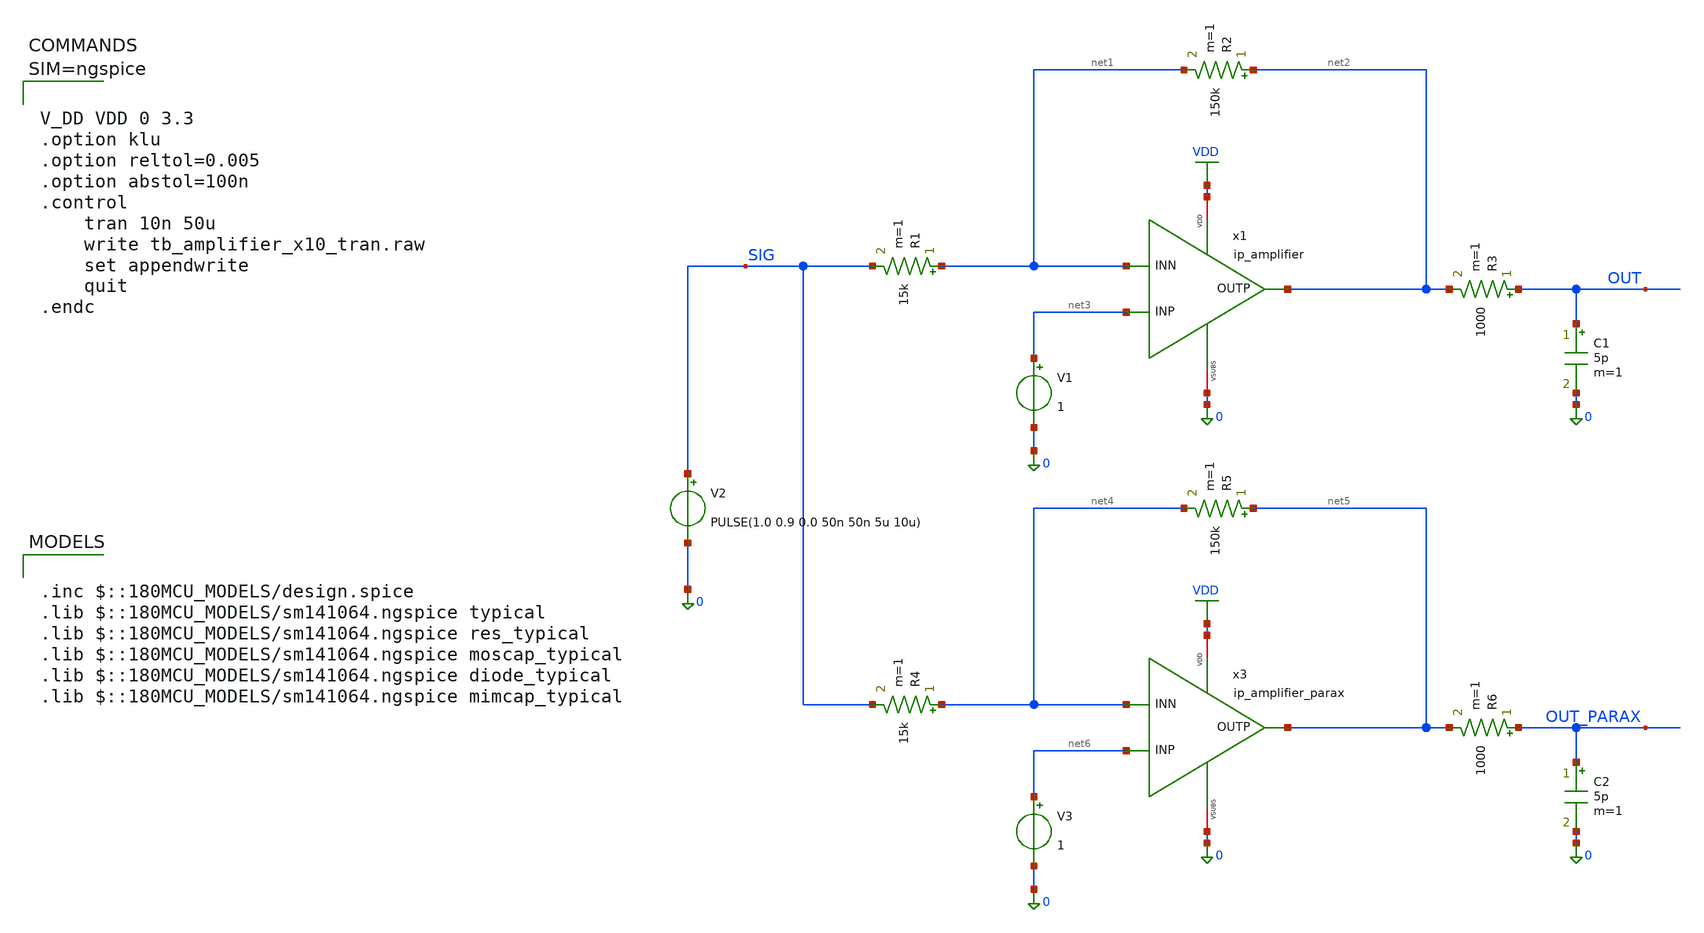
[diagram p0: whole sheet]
** sch_path: xschem/tb_amplifier_x10_tran.sch
**.subckt tb_amplifier_x10_tran
V2 SIG 0 PULSE(1.0 0.9 0.0 50n 50n 5u 10u)
x1 VDD 0 net3 net1 net2 ip_amplifier
R1 net1 SIG 15k m=1
R2 net2 net1 150k m=1
V1 net3 0 1
R3 OUT net2 1000 m=1
C1 OUT 0 5p m=1
R4 net4 SIG 15k m=1
R5 net5 net4 150k m=1
V3 net6 0 1
R6 OUT_PARAX net5 1000 m=1
C2 OUT_PARAX 0 5p m=1
x3 VDD 0 net6 net4 net5 ip_amplifier_parax
**** begin user architecture code

.inc $::180MCU_MODELS/design.spice
.lib $::180MCU_MODELS/sm141064.ngspice typical
.lib $::180MCU_MODELS/sm141064.ngspice res_typical
.lib $::180MCU_MODELS/sm141064.ngspice moscap_typical
.lib $::180MCU_MODELS/sm141064.ngspice diode_typical
.lib $::180MCU_MODELS/sm141064.ngspice mimcap_typical




V_DD VDD 0 3.3
.option klu
.option reltol=0.005
.option abstol=100n
.control
	tran 10n 50u
	write tb_amplifier_x10_tran.raw
	set appendwrite
	quit
.endc



**** end user architecture code
**.ends

* expanding   symbol:  ip_amplifier.sym # of pins=5
** sym_path: ip_amplifier.sym
** sch_path: ip_amplifier.sch
.subckt ip_amplifier VDD VSUBS INP INN OUTP
*.iopin VDD
*.iopin VSUBS
*.ipin INP
*.ipin INN
*.opin OUTP
XM1 COMP INP COMMON_ VDD pfet_03v3 L=5u W=18.0u nf=1 ad='int((nf+1)/2) * W/nf * 0.18u' as='int((nf+2)/2) * W/nf * 0.18u'
+ pd='2*int((nf+1)/2) * (W/nf + 0.18u)' ps='2*int((nf+2)/2) * (W/nf + 0.18u)' nrd='0.18u / W' nrs='0.18u / W'
+ sa=0 sb=0 sd=0 m=1 par=1
XM2 net6 INN COMMON_ VDD pfet_03v3 L=5u W=18.0u nf=1 ad='int((nf+1)/2) * W/nf * 0.18u' as='int((nf+2)/2) * W/nf * 0.18u'
+ pd='2*int((nf+1)/2) * (W/nf + 0.18u)' ps='2*int((nf+2)/2) * (W/nf + 0.18u)' nrd='0.18u / W' nrs='0.18u / W'
+ sa=0 sb=0 sd=0 m=1 par=1
XM3 net2 NBIAS VSUBS vsubs nfet_03v3 L=2u W=6u nf=1 ad='int((nf+1)/2) * W/nf * 0.18u' as='int((nf+2)/2) * W/nf * 0.18u'
+ pd='2*int((nf+1)/2) * (W/nf + 0.18u)' ps='2*int((nf+2)/2) * (W/nf + 0.18u)' nrd='0.18u / W' nrs='0.18u / W'
+ sa=0 sb=0 sd=0 m=2 par=2
XM4 net1 NBIAS VSUBS vsubs nfet_03v3 L=2u W=6u nf=1 ad='int((nf+1)/2) * W/nf * 0.18u' as='int((nf+2)/2) * W/nf * 0.18u'
+ pd='2*int((nf+1)/2) * (W/nf + 0.18u)' ps='2*int((nf+2)/2) * (W/nf + 0.18u)' nrd='0.18u / W' nrs='0.18u / W'
+ sa=0 sb=0 sd=0 m=1 par=1
XM7 NBIAS NBIAS net2 vsubs nfet_03v3 L=0.5u W=6u nf=1 ad='int((nf+1)/2) * W/nf * 0.18u' as='int((nf+2)/2) * W/nf * 0.18u'
+ pd='2*int((nf+1)/2) * (W/nf + 0.18u)' ps='2*int((nf+2)/2) * (W/nf + 0.18u)' nrd='0.18u / W' nrs='0.18u / W'
+ sa=0 sb=0 sd=0 m=4 par=4
XM8 net3 NBIAS net1 vsubs nfet_03v3 L=0.5u W=6u nf=1 ad='int((nf+1)/2) * W/nf * 0.18u' as='int((nf+2)/2) * W/nf * 0.18u'
+ pd='2*int((nf+1)/2) * (W/nf + 0.18u)' ps='2*int((nf+2)/2) * (W/nf + 0.18u)' nrd='0.18u / W' nrs='0.18u / W'
+ sa=0 sb=0 sd=0 m=4 par=4
XM9 net4 PBIAS VDD VDD pfet_03v3 L=2u W=6u nf=1 ad='int((nf+1)/2) * W/nf * 0.18u' as='int((nf+2)/2) * W/nf * 0.18u'
+ pd='2*int((nf+1)/2) * (W/nf + 0.18u)' ps='2*int((nf+2)/2) * (W/nf + 0.18u)' nrd='0.18u / W' nrs='0.18u / W'
+ sa=0 sb=0 sd=0 m=1 par=1
XM10 net5 PBIAS VDD VDD pfet_03v3 L=2u W=6u nf=1 ad='int((nf+1)/2) * W/nf * 0.18u' as='int((nf+2)/2) * W/nf * 0.18u'
+ pd='2*int((nf+1)/2) * (W/nf + 0.18u)' ps='2*int((nf+2)/2) * (W/nf + 0.18u)' nrd='0.18u / W' nrs='0.18u / W'
+ sa=0 sb=0 sd=0 m=1 par=1
XM11 PBIAS PBIAS net4 VDD pfet_03v3 L=0.5u W=6u nf=1 ad='int((nf+1)/2) * W/nf * 0.18u' as='int((nf+2)/2) * W/nf * 0.18u'
+ pd='2*int((nf+1)/2) * (W/nf + 0.18u)' ps='2*int((nf+2)/2) * (W/nf + 0.18u)' nrd='0.18u / W' nrs='0.18u / W'
+ sa=0 sb=0 sd=0 m=4 par=4
XM12 COMMON PBIAS net5 VDD pfet_03v3 L=0.5u W=6u nf=1 ad='int((nf+1)/2) * W/nf * 0.18u' as='int((nf+2)/2) * W/nf * 0.18u'
+ pd='2*int((nf+1)/2) * (W/nf + 0.18u)' ps='2*int((nf+2)/2) * (W/nf + 0.18u)' nrd='0.18u / W' nrs='0.18u / W'
+ sa=0 sb=0 sd=0 m=4 par=4
XM13 COMP net6 VSUBS vsubs nfet_03v3 L=5u W=6u nf=1 ad='int((nf+1)/2) * W/nf * 0.18u' as='int((nf+2)/2) * W/nf * 0.18u'
+ pd='2*int((nf+1)/2) * (W/nf + 0.18u)' ps='2*int((nf+2)/2) * (W/nf + 0.18u)' nrd='0.18u / W' nrs='0.18u / W'
+ sa=0 sb=0 sd=0 m=1 par=1
XM14 net6 net6 VSUBS vsubs nfet_03v3 L=5u W=6u nf=1 ad='int((nf+1)/2) * W/nf * 0.18u' as='int((nf+2)/2) * W/nf * 0.18u'
+ pd='2*int((nf+1)/2) * (W/nf + 0.18u)' ps='2*int((nf+2)/2) * (W/nf + 0.18u)' nrd='0.18u / W' nrs='0.18u / W'
+ sa=0 sb=0 sd=0 m=1 par=1
XM17 net8 PBIAS VDD VDD pfet_03v3 L=0.5u W=12u nf=1 ad='int((nf+1)/2) * W/nf * 0.18u' as='int((nf+2)/2) * W/nf * 0.18u'
+ pd='2*int((nf+1)/2) * (W/nf + 0.18u)' ps='2*int((nf+2)/2) * (W/nf + 0.18u)' nrd='0.18u / W' nrs='0.18u / W'
+ sa=0 sb=0 sd=0 m=2 par=2
XM18 OUTP COMP VSUBS vsubs nfet_03v3 L=0.5u W=12u nf=1 ad='int((nf+1)/2) * W/nf * 0.18u' as='int((nf+2)/2) * W/nf * 0.18u'
+ pd='2*int((nf+1)/2) * (W/nf + 0.18u)' ps='2*int((nf+2)/2) * (W/nf + 0.18u)' nrd='0.18u / W' nrs='0.18u / W'
+ sa=0 sb=0 sd=0 m=4 par=4
XR3 NBIAS net7 vsubs ppolyf_u_1k r_width=1e-6 r_length=48e-6 m=1
Vmeas VDD net7 0
Vmeas1 PBIAS net3 0
Vmeas2 COMMON COMMON_ 0
Vmeas3 net8 OUTP 0
XC1 OUTP COMP cap_mim_2f0_m2m3_noshield c_width=10e-6 c_length=10e-6 m=2
.ends


* expanding   symbol:  ip_amplifier_parax.sym # of pins=5
** sym_path: ip_amplifier.sym
.include [file normalize ./parax/ip_amplifier.sim.spice]
.GLOBAL VDD
.end
